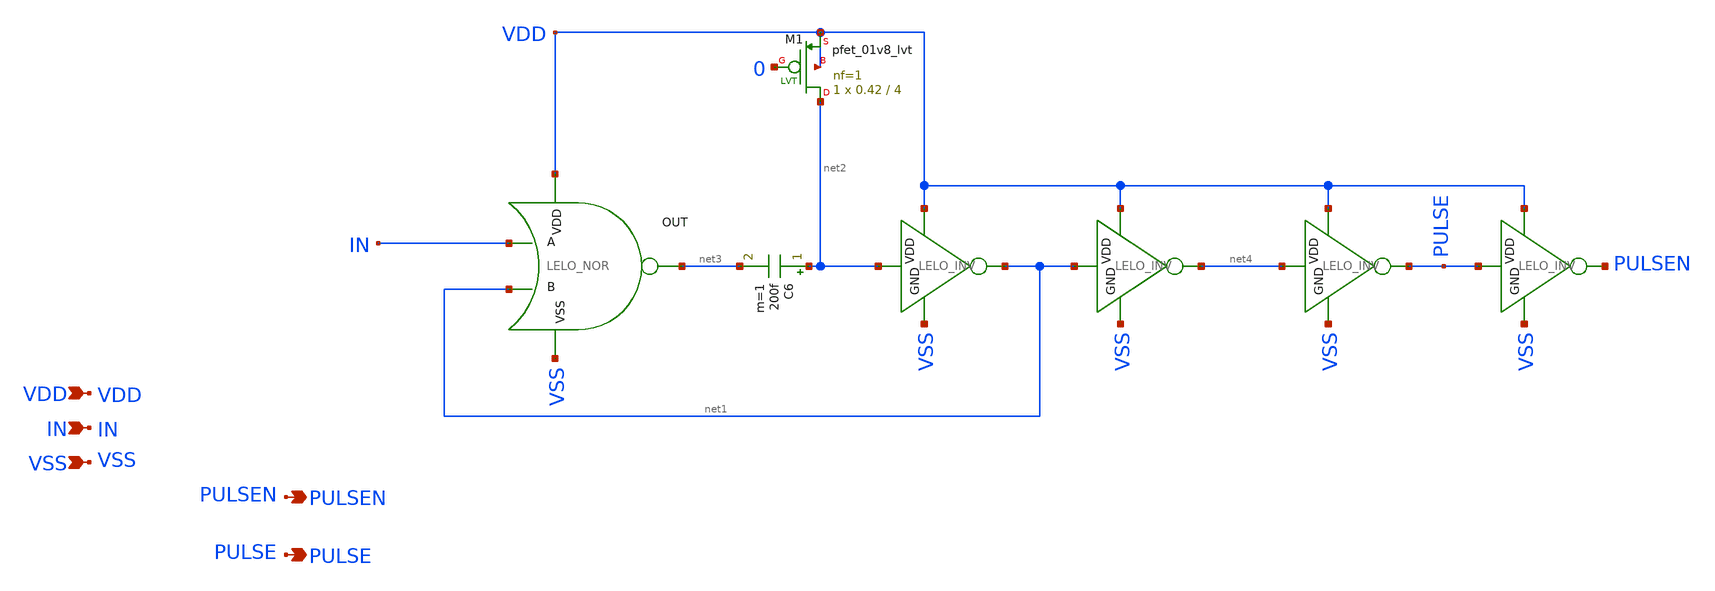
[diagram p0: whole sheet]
** sch_path: design/LELO_SVOD_SKY130A/LELO_ONESHOT2.sch
**.subckt LELO_ONESHOT2 VDD IN VSS PULSEN PULSE
*.ipin VDD
*.ipin IN
*.ipin VSS
*.opin PULSEN
*.opin PULSE
x12 VDD net3 IN net1 VSS LELO_NOR
C6 net2 net3 200f m=1
x13 VDD net2 net1 VSS LELO_INV
XM1 net2 0 VDD VDD sky130_fd_pr__pfet_01v8_lvt L=4 W=0.42 nf=1 ad='int((1 + 1)/2) * 0.42 / 1 * 0.29'
+ as='int((1 + 2)/2) * 0.42 / 1 * 0.29' pd='2*int((1 + 1)/2) * (0.42 / 1 + 0.29)' ps='2*int((1 + 2)/2) * (0.42 / 1 + 0.29)'
+ nrd='0.29 / 0.42 ' nrs='0.29 / 0.42 ' sa=0 sb=0 sd=0 mult=1 m=1
x1 VDD net1 net4 VSS LELO_INV
x2 VDD net4 PULSE VSS LELO_INV
x3 VDD PULSE PULSEN VSS LELO_INV
**.ends

* expanding   symbol:  LELO_SVOD_SKY130A/LELO_NOR.sym # of pins=5
** sym_path: design/LELO_SVOD_SKY130A/LELO_NOR.sym
** sch_path: design/LELO_SVOD_SKY130A/LELO_NOR.sch
.subckt LELO_NOR VDD OUT A B VSS
*.ipin VDD
*.ipin VSS
*.opin OUT
*.ipin A
*.ipin B
XM2 OUT B VSS VSS sky130_fd_pr__nfet_01v8 L=0.15 W=2 nf=1 ad='int((1 + 1)/2) * 2 / 1 * 0.29' as='int((1 + 2)/2) * 2 / 1 * 0.29'
+ pd='2*int((1 + 1)/2) * (2 / 1 + 0.29)' ps='2*int((1 + 2)/2) * (2 / 1 + 0.29)' nrd='0.29 / 2 ' nrs='0.29 / 2 '
+ sa=0 sb=0 sd=0 mult=1 m=1
XM1 OUT A VSS VSS sky130_fd_pr__nfet_01v8 L=0.15 W=2 nf=1 ad='int((1 + 1)/2) * 2 / 1 * 0.29' as='int((1 + 2)/2) * 2 / 1 * 0.29'
+ pd='2*int((1 + 1)/2) * (2 / 1 + 0.29)' ps='2*int((1 + 2)/2) * (2 / 1 + 0.29)' nrd='0.29 / 2 ' nrs='0.29 / 2 '
+ sa=0 sb=0 sd=0 mult=1 m=1
XM3 OUT B net1 VDD sky130_fd_pr__pfet_01v8 L=0.15 W=4 nf=1 ad='int((1 + 1)/2) * 4 / 1 * 0.29' as='int((1 + 2)/2) * 4 / 1 * 0.29'
+ pd='2*int((1 + 1)/2) * (4 / 1 + 0.29)' ps='2*int((1 + 2)/2) * (4 / 1 + 0.29)' nrd='0.29 / 4 ' nrs='0.29 / 4 '
+ sa=0 sb=0 sd=0 mult=1 m=1
XM4 net1 A VDD VDD sky130_fd_pr__pfet_01v8 L=0.15 W=4 nf=1 ad='int((1 + 1)/2) * 4 / 1 * 0.29' as='int((1 + 2)/2) * 4 / 1 * 0.29'
+ pd='2*int((1 + 1)/2) * (4 / 1 + 0.29)' ps='2*int((1 + 2)/2) * (4 / 1 + 0.29)' nrd='0.29 / 4 ' nrs='0.29 / 4 '
+ sa=0 sb=0 sd=0 mult=1 m=1
.ends


* expanding   symbol:  LELO_SVOD_SKY130A/LELO_INV.sym # of pins=4
** sym_path: design/LELO_SVOD_SKY130A/LELO_INV.sym
** sch_path: design/LELO_SVOD_SKY130A/LELO_INV.sch
.subckt LELO_INV VDD VIN VOUT GND
*.ipin VIN
*.ipin VDD
*.ipin GND
*.opin VOUT
XM1 VOUT VIN GND GND sky130_fd_pr__nfet_01v8_lvt L=0.15 W=1 nf=1 ad='int((1 + 1)/2) * 1 / 1 * 0.29' as='int((1 + 2)/2) * 1 / 1 * 0.29'
+ pd='2*int((1 + 1)/2) * (1 / 1 + 0.29)' ps='2*int((1 + 2)/2) * (1 / 1 + 0.29)' nrd='0.29 / 1 ' nrs='0.29 / 1 '
+ sa=0 sb=0 sd=0 mult=1 m=1
XM2 VOUT VIN VDD VDD sky130_fd_pr__pfet_01v8_lvt L=0.35 W=1 nf=1 ad='int((1 + 1)/2) * 1 / 1 * 0.29' as='int((1 + 2)/2) * 1 / 1 * 0.29'
+ pd='2*int((1 + 1)/2) * (1 / 1 + 0.29)' ps='2*int((1 + 2)/2) * (1 / 1 + 0.29)' nrd='0.29 / 1 ' nrs='0.29 / 1 '
+ sa=0 sb=0 sd=0 mult=2 m=2
.ends

.end
